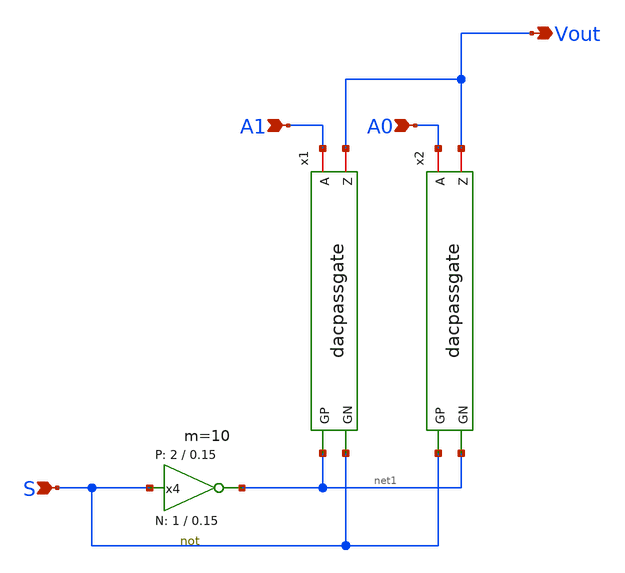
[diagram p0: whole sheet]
** sch_path: 2x1analogmux.sch
* Copyright 2021 Stefan Frederik Schippers
* Licensed under the Apache License, Version 2.0 (the "License");
* you may not use this file except in compliance with the License.
* You may obtain a copy of the License at
* https://www.apache.org/licenses/LICENSE-2.0
* Unless required by applicable law or agreed to in writing, software
* distributed under the License is distributed on an "AS IS" BASIS,
* WITHOUT WARRANTIES OR CONDITIONS OF ANY KIND, either express or implied.
* See the License for the specific language governing permissions and
* limitations under the License.
**.subckt 2x1analogmux S Vout A1 A0
*.ipin S
*.opin Vout
*.ipin A1
*.ipin A0
x1 net1 A1 Vout S dacpassgate
x2 S A0 Vout net1 dacpassgate
x4 net1 S VDD GND not W_N=1 L_N=0.15 W_P=2 L_P=0.15 m=10
**.ends

* expanding   symbol:  dacpassgate.sym # of pins=4
** sym_path: dacpassgate.sym
** sch_path: dacpassgate.sch
.subckt dacpassgate GP A Z GN
*.iopin A
*.iopin Z
*.ipin GP
*.ipin GN
XM1 net1 GN A GND sky130_fd_pr__nfet_01v8 L=0.5 W=1 nf=1 ad='int((nf+1)/2) * W/nf * 0.29' as='int((nf+2)/2) * W/nf * 0.29'
+ pd='2*int((nf+1)/2) * (W/nf + 0.29)' ps='2*int((nf+2)/2) * (W/nf + 0.29)' nrd='0.29 / W' nrs='0.29 / W'
+ sa=0 sb=0 sd=0 mult=10 m=10
XM2 net2 GP A VDD sky130_fd_pr__pfet_01v8 L=0.5 W=2 nf=1 ad='int((nf+1)/2) * W/nf * 0.29' as='int((nf+2)/2) * W/nf * 0.29'
+ pd='2*int((nf+1)/2) * (W/nf + 0.29)' ps='2*int((nf+2)/2) * (W/nf + 0.29)' nrd='0.29 / W' nrs='0.29 / W'
+ sa=0 sb=0 sd=0 mult=10 m=10
vidp net2 Z 0
vidn Z net1 0
.ends


* expanding   symbol:  sky130_tests/not.sym # of pins=2
** sym_path: sky130_tests/not.sym
** sch_path: sky130_tests/not.sch
.subckt not y a VCCPIN VSSPIN     W_N=1 L_N=0.15 W_P=2 L_P=0.15
*.opin y
*.ipin a
XM1 DN a VSSPIN VSSPIN sky130_fd_pr__nfet_01v8 L=L_N W=W_N nf=1 ad='int((1 + 1)/2) * W_N / 1 * 0.29'
+ as='int((1 + 2)/2) * W_N / 1 * 0.29' pd='2*int((1 + 1)/2) * (W_N / 1 + 0.29)' ps='2*int((1 + 2)/2) * (W_N / 1 + 0.29)'
+ nrd='0.29 / W_N ' nrs='0.29 / W_N ' sa=0 sb=0 sd=0 mult=1 m=1
XM2 DP a VCCPIN VCCPIN sky130_fd_pr__pfet_01v8 L=L_P W=W_P nf=1 ad='int((nf+1)/2) * W/nf * 0.29' as='int((nf+2)/2) * W/nf * 0.29'
+ pd='2*int((nf+1)/2) * (W/nf + 0.29)' ps='2*int((nf+2)/2) * (W/nf + 0.29)' nrd='0.29 / W' nrs='0.29 / W'
+ sa=0 sb=0 sd=0 mult=1 m=1
Vmeas DP y 0
.save i(vmeas)
Vmeas1 y DN 0
.save i(vmeas1)
.save v(dp)
.save v(dn)
.ends

.end
